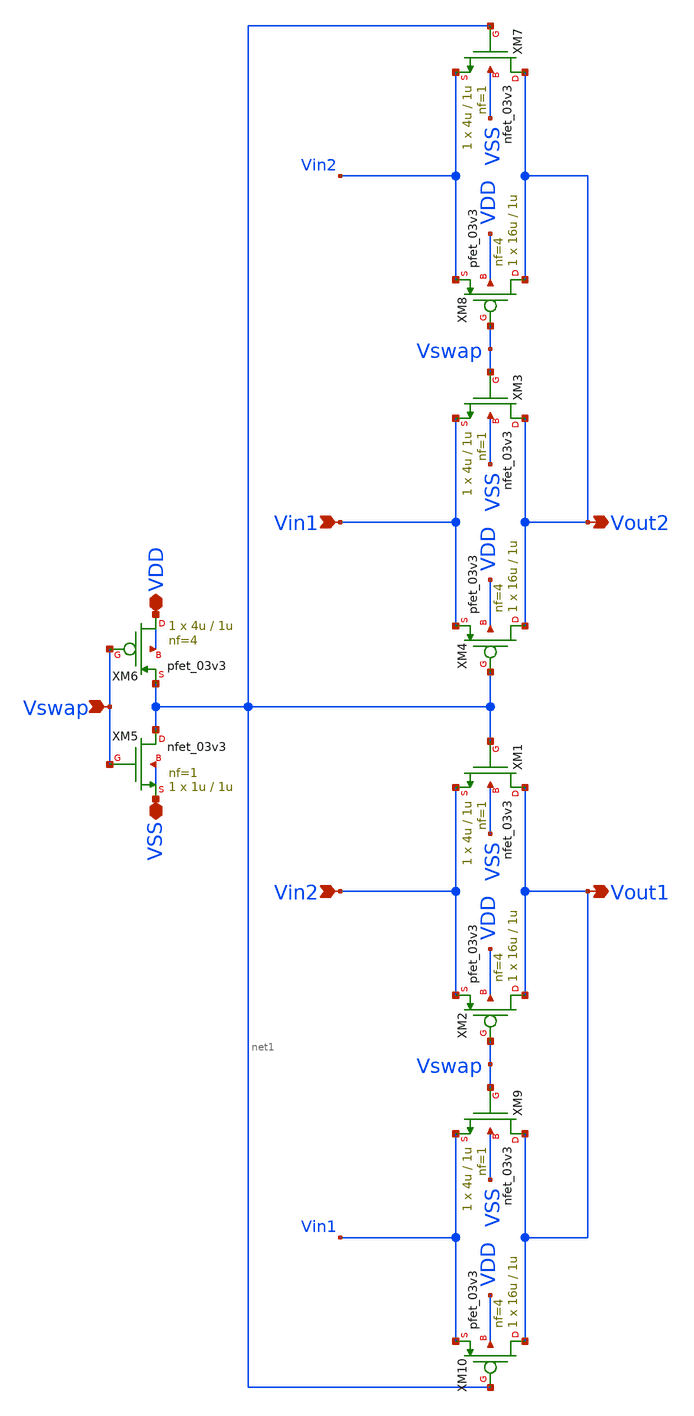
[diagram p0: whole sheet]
** sch_path: blocks/pll/mux.sch
**.subckt mux Vin1 Vout1 Vin2 Vout2 VDD VSS Vswap
*.ipin Vin1
*.opin Vout1
*.ipin Vin2
*.opin Vout2
*.iopin VDD
*.iopin VSS
*.ipin Vswap
XM1 Vout1 net1 Vin2 VSS nfet_03v3 L=1u W=4u nf=1 ad='int((nf+1)/2) * W/nf * 0.18u' as='int((nf+2)/2) * W/nf * 0.18u'
+ pd='2*int((nf+1)/2) * (W/nf + 0.18u)' ps='2*int((nf+2)/2) * (W/nf + 0.18u)' nrd='0.18u / W' nrs='0.18u / W'
+ sa=0 sb=0 sd=0 m=1
XM2 Vout1 Vswap Vin2 VDD pfet_03v3 L=1u W=16u nf=4 ad='int((nf+1)/2) * W/nf * 0.18u' as='int((nf+2)/2) * W/nf * 0.18u'
+ pd='2*int((nf+1)/2) * (W/nf + 0.18u)' ps='2*int((nf+2)/2) * (W/nf + 0.18u)' nrd='0.18u / W' nrs='0.18u / W'
+ sa=0 sb=0 sd=0 m=1
XM3 Vout2 Vswap Vin1 VSS nfet_03v3 L=1u W=4u nf=1 ad='int((nf+1)/2) * W/nf * 0.18u' as='int((nf+2)/2) * W/nf * 0.18u'
+ pd='2*int((nf+1)/2) * (W/nf + 0.18u)' ps='2*int((nf+2)/2) * (W/nf + 0.18u)' nrd='0.18u / W' nrs='0.18u / W'
+ sa=0 sb=0 sd=0 m=1
XM4 Vout2 net1 Vin1 VDD pfet_03v3 L=1u W=16u nf=4 ad='int((nf+1)/2) * W/nf * 0.18u' as='int((nf+2)/2) * W/nf * 0.18u'
+ pd='2*int((nf+1)/2) * (W/nf + 0.18u)' ps='2*int((nf+2)/2) * (W/nf + 0.18u)' nrd='0.18u / W' nrs='0.18u / W'
+ sa=0 sb=0 sd=0 m=1
XM5 net1 Vswap VSS VSS nfet_03v3 L=1u W=1u nf=1 ad='int((nf+1)/2) * W/nf * 0.18u' as='int((nf+2)/2) * W/nf * 0.18u'
+ pd='2*int((nf+1)/2) * (W/nf + 0.18u)' ps='2*int((nf+2)/2) * (W/nf + 0.18u)' nrd='0.18u / W' nrs='0.18u / W'
+ sa=0 sb=0 sd=0 m=1
XM6 VDD Vswap net1 VDD pfet_03v3 L=1u W=4u nf=4 ad='int((nf+1)/2) * W/nf * 0.18u' as='int((nf+2)/2) * W/nf * 0.18u'
+ pd='2*int((nf+1)/2) * (W/nf + 0.18u)' ps='2*int((nf+2)/2) * (W/nf + 0.18u)' nrd='0.18u / W' nrs='0.18u / W'
+ sa=0 sb=0 sd=0 m=1
XM7 Vout2 net1 Vin2 VSS nfet_03v3 L=1u W=4u nf=1 ad='int((nf+1)/2) * W/nf * 0.18u' as='int((nf+2)/2) * W/nf * 0.18u'
+ pd='2*int((nf+1)/2) * (W/nf + 0.18u)' ps='2*int((nf+2)/2) * (W/nf + 0.18u)' nrd='0.18u / W' nrs='0.18u / W'
+ sa=0 sb=0 sd=0 m=1
XM8 Vout2 Vswap Vin2 VDD pfet_03v3 L=1u W=16u nf=4 ad='int((nf+1)/2) * W/nf * 0.18u' as='int((nf+2)/2) * W/nf * 0.18u'
+ pd='2*int((nf+1)/2) * (W/nf + 0.18u)' ps='2*int((nf+2)/2) * (W/nf + 0.18u)' nrd='0.18u / W' nrs='0.18u / W'
+ sa=0 sb=0 sd=0 m=1
XM9 Vout1 Vswap Vin1 VSS nfet_03v3 L=1u W=4u nf=1 ad='int((nf+1)/2) * W/nf * 0.18u' as='int((nf+2)/2) * W/nf * 0.18u'
+ pd='2*int((nf+1)/2) * (W/nf + 0.18u)' ps='2*int((nf+2)/2) * (W/nf + 0.18u)' nrd='0.18u / W' nrs='0.18u / W'
+ sa=0 sb=0 sd=0 m=1
XM10 Vout1 net1 Vin1 VDD pfet_03v3 L=1u W=16u nf=4 ad='int((nf+1)/2) * W/nf * 0.18u' as='int((nf+2)/2) * W/nf * 0.18u'
+ pd='2*int((nf+1)/2) * (W/nf + 0.18u)' ps='2*int((nf+2)/2) * (W/nf + 0.18u)' nrd='0.18u / W' nrs='0.18u / W'
+ sa=0 sb=0 sd=0 m=1
**.ends
.end
